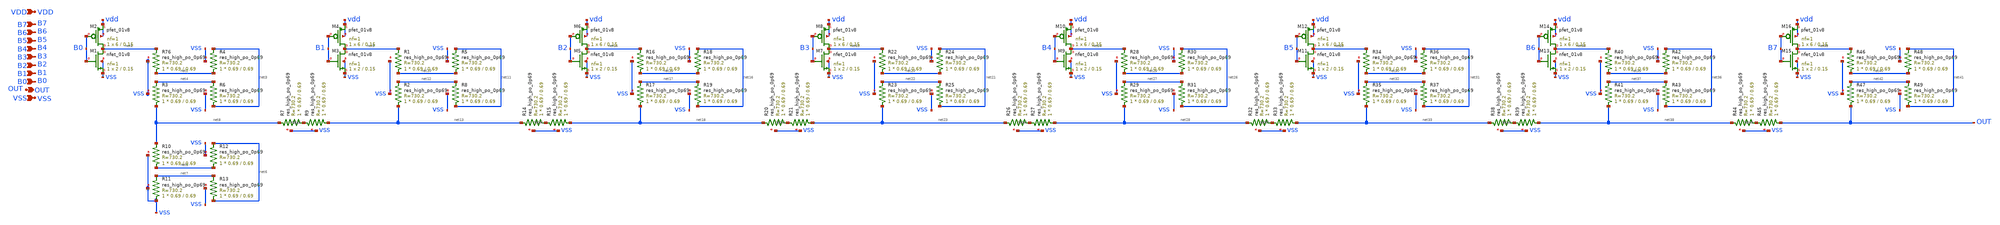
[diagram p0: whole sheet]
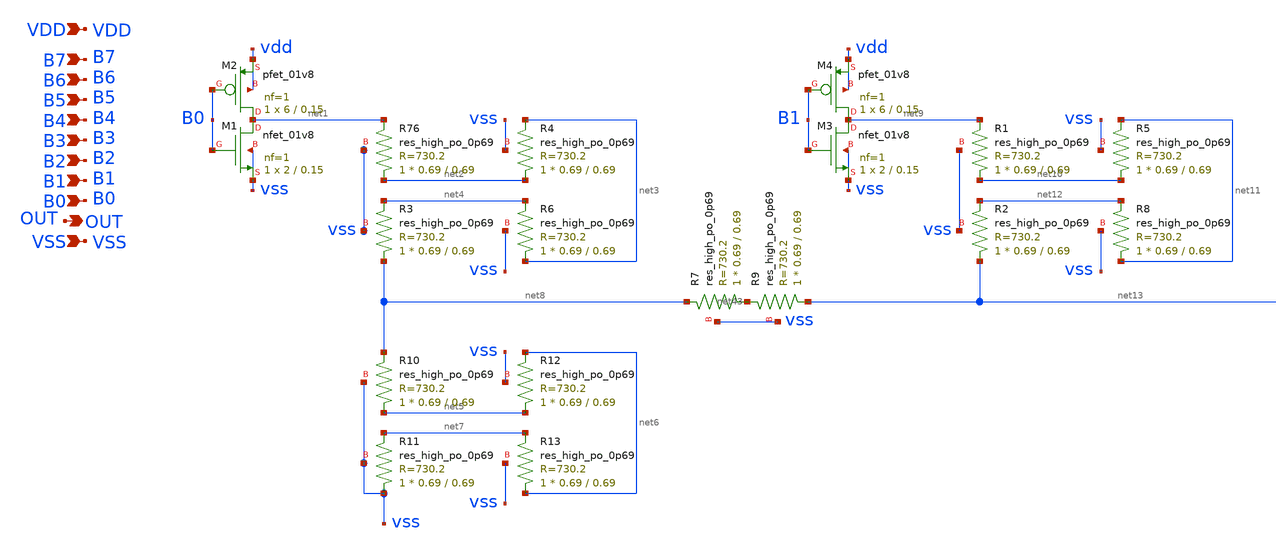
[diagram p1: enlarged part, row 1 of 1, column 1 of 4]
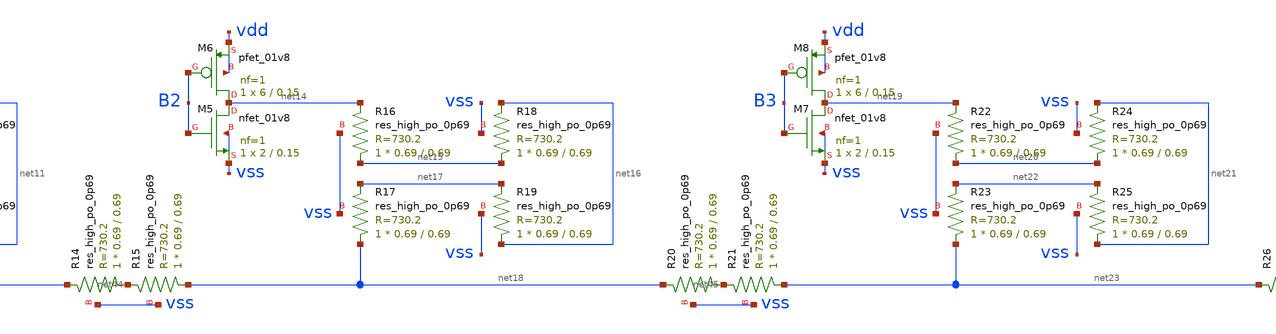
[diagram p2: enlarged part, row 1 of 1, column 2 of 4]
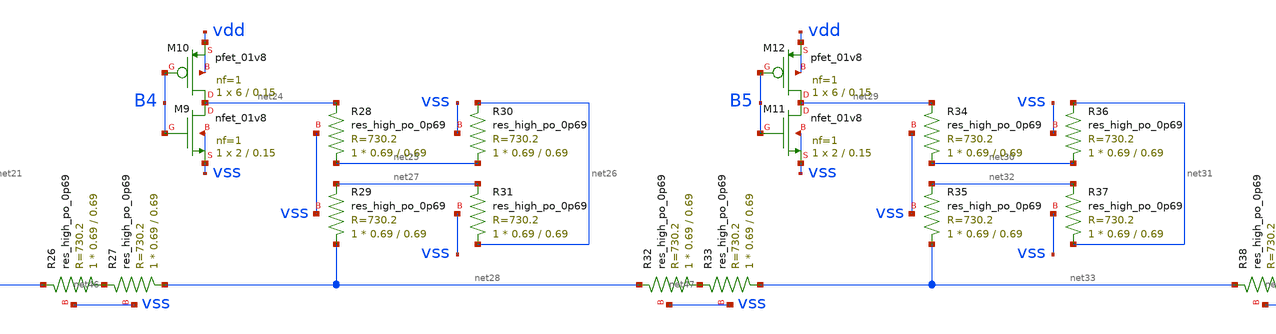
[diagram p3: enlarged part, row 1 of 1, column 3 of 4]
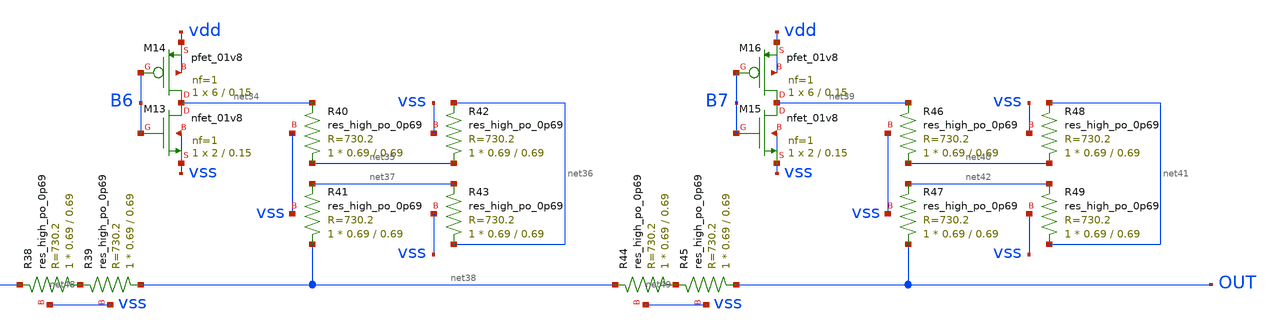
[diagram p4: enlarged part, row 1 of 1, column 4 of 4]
** sch_path: xschem/r2r_dac.sch
**.subckt r2r_dac VDD VSS B7 B6 B5 B4 B3 B2 B1 B0 OUT
*.ipin VDD
*.ipin VSS
*.ipin B7
*.ipin B6
*.ipin B5
*.ipin B4
*.ipin B3
*.ipin B2
*.ipin B1
*.ipin B0
*.opin OUT
XM1 net1 B0 vss vss sky130_fd_pr__nfet_01v8 L=0.15 W=2 nf=1 ad='int((nf+1)/2) * W/nf * 0.29' as='int((nf+2)/2) * W/nf * 0.29'
+ pd='2*int((nf+1)/2) * (W/nf + 0.29)' ps='2*int((nf+2)/2) * (W/nf + 0.29)' nrd='0.29 / W' nrs='0.29 / W'
+ sa=0 sb=0 sd=0 mult=1 m=1
XM2 net1 B0 vdd vdd sky130_fd_pr__pfet_01v8 L=0.15 W=6 nf=1 ad='int((nf+1)/2) * W/nf * 0.29' as='int((nf+2)/2) * W/nf * 0.29'
+ pd='2*int((nf+1)/2) * (W/nf + 0.29)' ps='2*int((nf+2)/2) * (W/nf + 0.29)' nrd='0.29 / W' nrs='0.29 / W'
+ sa=0 sb=0 sd=0 mult=1 m=1
XR76 net2 net1 vss sky130_fd_pr__res_high_po_0p69 L=0.69 mult=1 m=1
XR3 net8 net4 vss sky130_fd_pr__res_high_po_0p69 L=0.69 mult=1 m=1
XR4 net2 net3 vss sky130_fd_pr__res_high_po_0p69 L=0.69 mult=1 m=1
XR6 net3 net4 vss sky130_fd_pr__res_high_po_0p69 L=0.69 mult=1 m=1
XR7 net43 net8 vss sky130_fd_pr__res_high_po_0p69 L=0.69 mult=1 m=1
XR9 net13 net43 vss sky130_fd_pr__res_high_po_0p69 L=0.69 mult=1 m=1
XR10 net5 net8 vss sky130_fd_pr__res_high_po_0p69 L=0.69 mult=1 m=1
XR11 vss net7 vss sky130_fd_pr__res_high_po_0p69 L=0.69 mult=1 m=1
XR12 net5 net6 vss sky130_fd_pr__res_high_po_0p69 L=0.69 mult=1 m=1
XR13 net6 net7 vss sky130_fd_pr__res_high_po_0p69 L=0.69 mult=1 m=1
XM3 net9 B1 vss vss sky130_fd_pr__nfet_01v8 L=0.15 W=2 nf=1 ad='int((nf+1)/2) * W/nf * 0.29' as='int((nf+2)/2) * W/nf * 0.29'
+ pd='2*int((nf+1)/2) * (W/nf + 0.29)' ps='2*int((nf+2)/2) * (W/nf + 0.29)' nrd='0.29 / W' nrs='0.29 / W'
+ sa=0 sb=0 sd=0 mult=1 m=1
XM4 net9 B1 vdd vdd sky130_fd_pr__pfet_01v8 L=0.15 W=6 nf=1 ad='int((nf+1)/2) * W/nf * 0.29' as='int((nf+2)/2) * W/nf * 0.29'
+ pd='2*int((nf+1)/2) * (W/nf + 0.29)' ps='2*int((nf+2)/2) * (W/nf + 0.29)' nrd='0.29 / W' nrs='0.29 / W'
+ sa=0 sb=0 sd=0 mult=1 m=1
XR1 net10 net9 vss sky130_fd_pr__res_high_po_0p69 L=0.69 mult=1 m=1
XR2 net13 net12 vss sky130_fd_pr__res_high_po_0p69 L=0.69 mult=1 m=1
XR5 net10 net11 vss sky130_fd_pr__res_high_po_0p69 L=0.69 mult=1 m=1
XR8 net11 net12 vss sky130_fd_pr__res_high_po_0p69 L=0.69 mult=1 m=1
XR14 net44 net13 vss sky130_fd_pr__res_high_po_0p69 L=0.69 mult=1 m=1
XR15 net18 net44 vss sky130_fd_pr__res_high_po_0p69 L=0.69 mult=1 m=1
XM5 net14 B2 vss vss sky130_fd_pr__nfet_01v8 L=0.15 W=2 nf=1 ad='int((nf+1)/2) * W/nf * 0.29' as='int((nf+2)/2) * W/nf * 0.29'
+ pd='2*int((nf+1)/2) * (W/nf + 0.29)' ps='2*int((nf+2)/2) * (W/nf + 0.29)' nrd='0.29 / W' nrs='0.29 / W'
+ sa=0 sb=0 sd=0 mult=1 m=1
XM6 net14 B2 vdd vdd sky130_fd_pr__pfet_01v8 L=0.15 W=6 nf=1 ad='int((nf+1)/2) * W/nf * 0.29' as='int((nf+2)/2) * W/nf * 0.29'
+ pd='2*int((nf+1)/2) * (W/nf + 0.29)' ps='2*int((nf+2)/2) * (W/nf + 0.29)' nrd='0.29 / W' nrs='0.29 / W'
+ sa=0 sb=0 sd=0 mult=1 m=1
XR16 net15 net14 vss sky130_fd_pr__res_high_po_0p69 L=0.69 mult=1 m=1
XR17 net18 net17 vss sky130_fd_pr__res_high_po_0p69 L=0.69 mult=1 m=1
XR18 net15 net16 vss sky130_fd_pr__res_high_po_0p69 L=0.69 mult=1 m=1
XR19 net16 net17 vss sky130_fd_pr__res_high_po_0p69 L=0.69 mult=1 m=1
XR20 net45 net18 vss sky130_fd_pr__res_high_po_0p69 L=0.69 mult=1 m=1
XR21 net23 net45 vss sky130_fd_pr__res_high_po_0p69 L=0.69 mult=1 m=1
XM7 net19 B3 vss vss sky130_fd_pr__nfet_01v8 L=0.15 W=2 nf=1 ad='int((nf+1)/2) * W/nf * 0.29' as='int((nf+2)/2) * W/nf * 0.29'
+ pd='2*int((nf+1)/2) * (W/nf + 0.29)' ps='2*int((nf+2)/2) * (W/nf + 0.29)' nrd='0.29 / W' nrs='0.29 / W'
+ sa=0 sb=0 sd=0 mult=1 m=1
XM8 net19 B3 vdd vdd sky130_fd_pr__pfet_01v8 L=0.15 W=6 nf=1 ad='int((nf+1)/2) * W/nf * 0.29' as='int((nf+2)/2) * W/nf * 0.29'
+ pd='2*int((nf+1)/2) * (W/nf + 0.29)' ps='2*int((nf+2)/2) * (W/nf + 0.29)' nrd='0.29 / W' nrs='0.29 / W'
+ sa=0 sb=0 sd=0 mult=1 m=1
XR22 net20 net19 vss sky130_fd_pr__res_high_po_0p69 L=0.69 mult=1 m=1
XR23 net23 net22 vss sky130_fd_pr__res_high_po_0p69 L=0.69 mult=1 m=1
XR24 net20 net21 vss sky130_fd_pr__res_high_po_0p69 L=0.69 mult=1 m=1
XR25 net21 net22 vss sky130_fd_pr__res_high_po_0p69 L=0.69 mult=1 m=1
XR26 net46 net23 vss sky130_fd_pr__res_high_po_0p69 L=0.69 mult=1 m=1
XR27 net28 net46 vss sky130_fd_pr__res_high_po_0p69 L=0.69 mult=1 m=1
XM9 net24 B4 vss vss sky130_fd_pr__nfet_01v8 L=0.15 W=2 nf=1 ad='int((nf+1)/2) * W/nf * 0.29' as='int((nf+2)/2) * W/nf * 0.29'
+ pd='2*int((nf+1)/2) * (W/nf + 0.29)' ps='2*int((nf+2)/2) * (W/nf + 0.29)' nrd='0.29 / W' nrs='0.29 / W'
+ sa=0 sb=0 sd=0 mult=1 m=1
XM10 net24 B4 vdd vdd sky130_fd_pr__pfet_01v8 L=0.15 W=6 nf=1 ad='int((nf+1)/2) * W/nf * 0.29' as='int((nf+2)/2) * W/nf * 0.29'
+ pd='2*int((nf+1)/2) * (W/nf + 0.29)' ps='2*int((nf+2)/2) * (W/nf + 0.29)' nrd='0.29 / W' nrs='0.29 / W'
+ sa=0 sb=0 sd=0 mult=1 m=1
XR28 net25 net24 vss sky130_fd_pr__res_high_po_0p69 L=0.69 mult=1 m=1
XR29 net28 net27 vss sky130_fd_pr__res_high_po_0p69 L=0.69 mult=1 m=1
XR30 net25 net26 vss sky130_fd_pr__res_high_po_0p69 L=0.69 mult=1 m=1
XR31 net26 net27 vss sky130_fd_pr__res_high_po_0p69 L=0.69 mult=1 m=1
XR32 net47 net28 vss sky130_fd_pr__res_high_po_0p69 L=0.69 mult=1 m=1
XR33 net33 net47 vss sky130_fd_pr__res_high_po_0p69 L=0.69 mult=1 m=1
XM11 net29 B5 vss vss sky130_fd_pr__nfet_01v8 L=0.15 W=2 nf=1 ad='int((nf+1)/2) * W/nf * 0.29' as='int((nf+2)/2) * W/nf * 0.29'
+ pd='2*int((nf+1)/2) * (W/nf + 0.29)' ps='2*int((nf+2)/2) * (W/nf + 0.29)' nrd='0.29 / W' nrs='0.29 / W'
+ sa=0 sb=0 sd=0 mult=1 m=1
XM12 net29 B5 vdd vdd sky130_fd_pr__pfet_01v8 L=0.15 W=6 nf=1 ad='int((nf+1)/2) * W/nf * 0.29' as='int((nf+2)/2) * W/nf * 0.29'
+ pd='2*int((nf+1)/2) * (W/nf + 0.29)' ps='2*int((nf+2)/2) * (W/nf + 0.29)' nrd='0.29 / W' nrs='0.29 / W'
+ sa=0 sb=0 sd=0 mult=1 m=1
XR34 net30 net29 vss sky130_fd_pr__res_high_po_0p69 L=0.69 mult=1 m=1
XR35 net33 net32 vss sky130_fd_pr__res_high_po_0p69 L=0.69 mult=1 m=1
XR36 net30 net31 vss sky130_fd_pr__res_high_po_0p69 L=0.69 mult=1 m=1
XR37 net31 net32 vss sky130_fd_pr__res_high_po_0p69 L=0.69 mult=1 m=1
XR38 net48 net33 vss sky130_fd_pr__res_high_po_0p69 L=0.69 mult=1 m=1
XR39 net38 net48 vss sky130_fd_pr__res_high_po_0p69 L=0.69 mult=1 m=1
XM13 net34 B6 vss vss sky130_fd_pr__nfet_01v8 L=0.15 W=2 nf=1 ad='int((nf+1)/2) * W/nf * 0.29' as='int((nf+2)/2) * W/nf * 0.29'
+ pd='2*int((nf+1)/2) * (W/nf + 0.29)' ps='2*int((nf+2)/2) * (W/nf + 0.29)' nrd='0.29 / W' nrs='0.29 / W'
+ sa=0 sb=0 sd=0 mult=1 m=1
XM14 net34 B6 vdd vdd sky130_fd_pr__pfet_01v8 L=0.15 W=6 nf=1 ad='int((nf+1)/2) * W/nf * 0.29' as='int((nf+2)/2) * W/nf * 0.29'
+ pd='2*int((nf+1)/2) * (W/nf + 0.29)' ps='2*int((nf+2)/2) * (W/nf + 0.29)' nrd='0.29 / W' nrs='0.29 / W'
+ sa=0 sb=0 sd=0 mult=1 m=1
XR40 net35 net34 vss sky130_fd_pr__res_high_po_0p69 L=0.69 mult=1 m=1
XR41 net38 net37 vss sky130_fd_pr__res_high_po_0p69 L=0.69 mult=1 m=1
XR42 net35 net36 vss sky130_fd_pr__res_high_po_0p69 L=0.69 mult=1 m=1
XR43 net36 net37 vss sky130_fd_pr__res_high_po_0p69 L=0.69 mult=1 m=1
XR44 net49 net38 vss sky130_fd_pr__res_high_po_0p69 L=0.69 mult=1 m=1
XR45 OUT net49 vss sky130_fd_pr__res_high_po_0p69 L=0.69 mult=1 m=1
XM15 net39 B7 vss vss sky130_fd_pr__nfet_01v8 L=0.15 W=2 nf=1 ad='int((nf+1)/2) * W/nf * 0.29' as='int((nf+2)/2) * W/nf * 0.29'
+ pd='2*int((nf+1)/2) * (W/nf + 0.29)' ps='2*int((nf+2)/2) * (W/nf + 0.29)' nrd='0.29 / W' nrs='0.29 / W'
+ sa=0 sb=0 sd=0 mult=1 m=1
XM16 net39 B7 vdd vdd sky130_fd_pr__pfet_01v8 L=0.15 W=6 nf=1 ad='int((nf+1)/2) * W/nf * 0.29' as='int((nf+2)/2) * W/nf * 0.29'
+ pd='2*int((nf+1)/2) * (W/nf + 0.29)' ps='2*int((nf+2)/2) * (W/nf + 0.29)' nrd='0.29 / W' nrs='0.29 / W'
+ sa=0 sb=0 sd=0 mult=1 m=1
XR46 net40 net39 vss sky130_fd_pr__res_high_po_0p69 L=0.69 mult=1 m=1
XR47 OUT net42 vss sky130_fd_pr__res_high_po_0p69 L=0.69 mult=1 m=1
XR48 net40 net41 vss sky130_fd_pr__res_high_po_0p69 L=0.69 mult=1 m=1
XR49 net41 net42 vss sky130_fd_pr__res_high_po_0p69 L=0.69 mult=1 m=1
**.ends
.end
